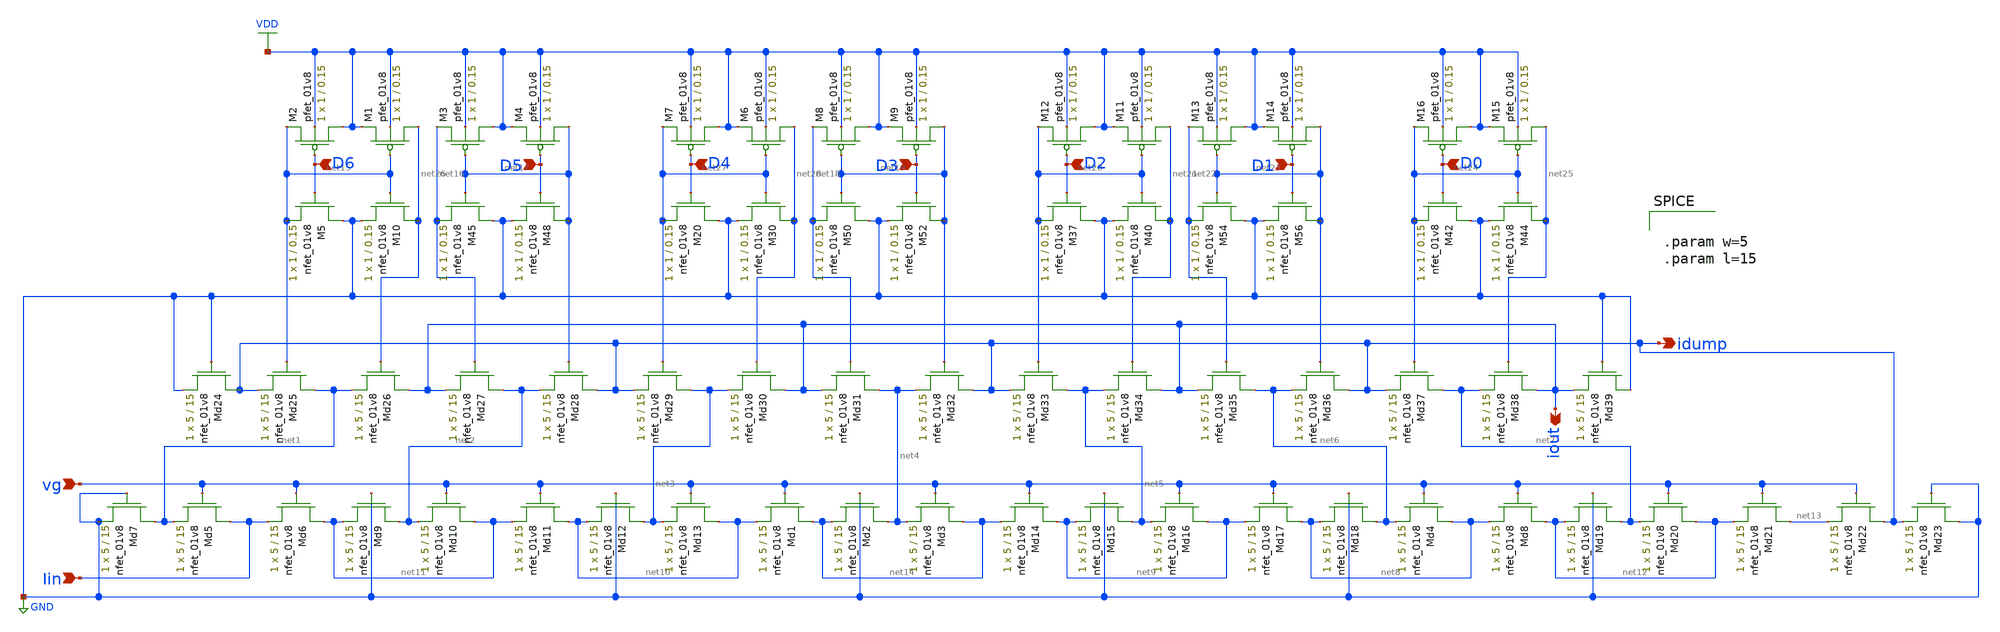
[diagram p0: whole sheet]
** sch_path: schematic/ladder_buffer_LDS4.sch
**.subckt ladder_buffer_LDS4 iout idump vg D0 D1 D3 D5 D6 Iin D4 D2
*.opin iout
*.opin idump
*.ipin vg
*.ipin D0
*.ipin D1
*.ipin D3
*.ipin D5
*.ipin D6
*.ipin Iin
*.ipin D4
*.ipin D2
XMd7 net1 GND GND GND sky130_fd_pr__nfet_01v8 L=15 W=5 nf=1 ad='int((nf+1)/2) * W/nf * 0.29' as='int((nf+2)/2) * W/nf * 0.29'
+ pd='2*int((nf+1)/2) * (W/nf + 0.29)' ps='2*int((nf+2)/2) * (W/nf + 0.29)' nrd='0.29 / W' nrs='0.29 / W'
+ sa=0 sb=0 sd=0 mult=1 m=1
XM5 GND D6 net15 GND sky130_fd_pr__nfet_01v8 L=0.15 W=1 nf=1 ad='int((nf+1)/2) * W/nf * 0.29' as='int((nf+2)/2) * W/nf * 0.29'
+ pd='2*int((nf+1)/2) * (W/nf + 0.29)' ps='2*int((nf+2)/2) * (W/nf + 0.29)' nrd='0.29 / W' nrs='0.29 / W'
+ sa=0 sb=0 sd=0 mult=1 m=1
XM10 net26 net15 GND GND sky130_fd_pr__nfet_01v8 L=0.15 W=1 nf=1 ad='int((nf+1)/2) * W/nf * 0.29' as='int((nf+2)/2) * W/nf * 0.29'
+ pd='2*int((nf+1)/2) * (W/nf + 0.29)' ps='2*int((nf+2)/2) * (W/nf + 0.29)' nrd='0.29 / W' nrs='0.29 / W'
+ sa=0 sb=0 sd=0 mult=1 m=1
XM20 GND D4 net27 GND sky130_fd_pr__nfet_01v8 L=0.15 W=1 nf=1 ad='int((nf+1)/2) * W/nf * 0.29' as='int((nf+2)/2) * W/nf * 0.29'
+ pd='2*int((nf+1)/2) * (W/nf + 0.29)' ps='2*int((nf+2)/2) * (W/nf + 0.29)' nrd='0.29 / W' nrs='0.29 / W'
+ sa=0 sb=0 sd=0 mult=1 m=1
XM30 net28 net27 GND GND sky130_fd_pr__nfet_01v8 L=0.15 W=1 nf=1 ad='int((nf+1)/2) * W/nf * 0.29' as='int((nf+2)/2) * W/nf * 0.29'
+ pd='2*int((nf+1)/2) * (W/nf + 0.29)' ps='2*int((nf+2)/2) * (W/nf + 0.29)' nrd='0.29 / W' nrs='0.29 / W'
+ sa=0 sb=0 sd=0 mult=1 m=1
XM37 GND D2 net20 GND sky130_fd_pr__nfet_01v8 L=0.15 W=1 nf=1 ad='int((nf+1)/2) * W/nf * 0.29' as='int((nf+2)/2) * W/nf * 0.29'
+ pd='2*int((nf+1)/2) * (W/nf + 0.29)' ps='2*int((nf+2)/2) * (W/nf + 0.29)' nrd='0.29 / W' nrs='0.29 / W'
+ sa=0 sb=0 sd=0 mult=1 m=1
XM40 net21 net20 GND GND sky130_fd_pr__nfet_01v8 L=0.15 W=1 nf=1 ad='int((nf+1)/2) * W/nf * 0.29' as='int((nf+2)/2) * W/nf * 0.29'
+ pd='2*int((nf+1)/2) * (W/nf + 0.29)' ps='2*int((nf+2)/2) * (W/nf + 0.29)' nrd='0.29 / W' nrs='0.29 / W'
+ sa=0 sb=0 sd=0 mult=1 m=1
XM42 GND D0 net24 GND sky130_fd_pr__nfet_01v8 L=0.15 W=1 nf=1 ad='int((nf+1)/2) * W/nf * 0.29' as='int((nf+2)/2) * W/nf * 0.29'
+ pd='2*int((nf+1)/2) * (W/nf + 0.29)' ps='2*int((nf+2)/2) * (W/nf + 0.29)' nrd='0.29 / W' nrs='0.29 / W'
+ sa=0 sb=0 sd=0 mult=1 m=1
XM44 net25 net24 GND GND sky130_fd_pr__nfet_01v8 L=0.15 W=1 nf=1 ad='int((nf+1)/2) * W/nf * 0.29' as='int((nf+2)/2) * W/nf * 0.29'
+ pd='2*int((nf+1)/2) * (W/nf + 0.29)' ps='2*int((nf+2)/2) * (W/nf + 0.29)' nrd='0.29 / W' nrs='0.29 / W'
+ sa=0 sb=0 sd=0 mult=1 m=1
XM45 GND net17 net16 GND sky130_fd_pr__nfet_01v8 L=0.15 W=1 nf=1 ad='int((nf+1)/2) * W/nf * 0.29' as='int((nf+2)/2) * W/nf * 0.29'
+ pd='2*int((nf+1)/2) * (W/nf + 0.29)' ps='2*int((nf+2)/2) * (W/nf + 0.29)' nrd='0.29 / W' nrs='0.29 / W'
+ sa=0 sb=0 sd=0 mult=1 m=1
XM48 net17 D5 GND GND sky130_fd_pr__nfet_01v8 L=0.15 W=1 nf=1 ad='int((nf+1)/2) * W/nf * 0.29' as='int((nf+2)/2) * W/nf * 0.29'
+ pd='2*int((nf+1)/2) * (W/nf + 0.29)' ps='2*int((nf+2)/2) * (W/nf + 0.29)' nrd='0.29 / W' nrs='0.29 / W'
+ sa=0 sb=0 sd=0 mult=1 m=1
XM50 GND net19 net18 GND sky130_fd_pr__nfet_01v8 L=0.15 W=1 nf=1 ad='int((nf+1)/2) * W/nf * 0.29' as='int((nf+2)/2) * W/nf * 0.29'
+ pd='2*int((nf+1)/2) * (W/nf + 0.29)' ps='2*int((nf+2)/2) * (W/nf + 0.29)' nrd='0.29 / W' nrs='0.29 / W'
+ sa=0 sb=0 sd=0 mult=1 m=1
XM52 net19 D3 GND GND sky130_fd_pr__nfet_01v8 L=0.15 W=1 nf=1 ad='int((nf+1)/2) * W/nf * 0.29' as='int((nf+2)/2) * W/nf * 0.29'
+ pd='2*int((nf+1)/2) * (W/nf + 0.29)' ps='2*int((nf+2)/2) * (W/nf + 0.29)' nrd='0.29 / W' nrs='0.29 / W'
+ sa=0 sb=0 sd=0 mult=1 m=1
XM54 GND net23 net22 GND sky130_fd_pr__nfet_01v8 L=0.15 W=1 nf=1 ad='int((nf+1)/2) * W/nf * 0.29' as='int((nf+2)/2) * W/nf * 0.29'
+ pd='2*int((nf+1)/2) * (W/nf + 0.29)' ps='2*int((nf+2)/2) * (W/nf + 0.29)' nrd='0.29 / W' nrs='0.29 / W'
+ sa=0 sb=0 sd=0 mult=1 m=1
XM56 net23 D1 GND GND sky130_fd_pr__nfet_01v8 L=0.15 W=1 nf=1 ad='int((nf+1)/2) * W/nf * 0.29' as='int((nf+2)/2) * W/nf * 0.29'
+ pd='2*int((nf+1)/2) * (W/nf + 0.29)' ps='2*int((nf+2)/2) * (W/nf + 0.29)' nrd='0.29 / W' nrs='0.29 / W'
+ sa=0 sb=0 sd=0 mult=1 m=1
XMd5 Iin vg net1 GND sky130_fd_pr__nfet_01v8 L=15 W=5 nf=1 ad='int((nf+1)/2) * W/nf * 0.29' as='int((nf+2)/2) * W/nf * 0.29'
+ pd='2*int((nf+1)/2) * (W/nf + 0.29)' ps='2*int((nf+2)/2) * (W/nf + 0.29)' nrd='0.29 / W' nrs='0.29 / W'
+ sa=0 sb=0 sd=0 mult=1 m=1
XMd6 net11 vg Iin GND sky130_fd_pr__nfet_01v8 L=15 W=5 nf=1 ad='int((nf+1)/2) * W/nf * 0.29' as='int((nf+2)/2) * W/nf * 0.29'
+ pd='2*int((nf+1)/2) * (W/nf + 0.29)' ps='2*int((nf+2)/2) * (W/nf + 0.29)' nrd='0.29 / W' nrs='0.29 / W'
+ sa=0 sb=0 sd=0 mult=1 m=1
XMd9 net2 GND net11 GND sky130_fd_pr__nfet_01v8 L=15 W=5 nf=1 ad='int((nf+1)/2) * W/nf * 0.29' as='int((nf+2)/2) * W/nf * 0.29'
+ pd='2*int((nf+1)/2) * (W/nf + 0.29)' ps='2*int((nf+2)/2) * (W/nf + 0.29)' nrd='0.29 / W' nrs='0.29 / W'
+ sa=0 sb=0 sd=0 mult=1 m=1
XMd10 net11 vg net2 GND sky130_fd_pr__nfet_01v8 L=15 W=5 nf=1 ad='int((nf+1)/2) * W/nf * 0.29' as='int((nf+2)/2) * W/nf * 0.29'
+ pd='2*int((nf+1)/2) * (W/nf + 0.29)' ps='2*int((nf+2)/2) * (W/nf + 0.29)' nrd='0.29 / W' nrs='0.29 / W'
+ sa=0 sb=0 sd=0 mult=1 m=1
XMd11 net10 vg net11 GND sky130_fd_pr__nfet_01v8 L=15 W=5 nf=1 ad='int((nf+1)/2) * W/nf * 0.29' as='int((nf+2)/2) * W/nf * 0.29'
+ pd='2*int((nf+1)/2) * (W/nf + 0.29)' ps='2*int((nf+2)/2) * (W/nf + 0.29)' nrd='0.29 / W' nrs='0.29 / W'
+ sa=0 sb=0 sd=0 mult=1 m=1
XMd12 net3 GND net10 GND sky130_fd_pr__nfet_01v8 L=15 W=5 nf=1 ad='int((nf+1)/2) * W/nf * 0.29' as='int((nf+2)/2) * W/nf * 0.29'
+ pd='2*int((nf+1)/2) * (W/nf + 0.29)' ps='2*int((nf+2)/2) * (W/nf + 0.29)' nrd='0.29 / W' nrs='0.29 / W'
+ sa=0 sb=0 sd=0 mult=1 m=1
XMd13 net10 vg net3 GND sky130_fd_pr__nfet_01v8 L=15 W=5 nf=1 ad='int((nf+1)/2) * W/nf * 0.29' as='int((nf+2)/2) * W/nf * 0.29'
+ pd='2*int((nf+1)/2) * (W/nf + 0.29)' ps='2*int((nf+2)/2) * (W/nf + 0.29)' nrd='0.29 / W' nrs='0.29 / W'
+ sa=0 sb=0 sd=0 mult=1 m=1
XMd1 net14 vg net10 GND sky130_fd_pr__nfet_01v8 L=15 W=5 nf=1 ad='int((nf+1)/2) * W/nf * 0.29' as='int((nf+2)/2) * W/nf * 0.29'
+ pd='2*int((nf+1)/2) * (W/nf + 0.29)' ps='2*int((nf+2)/2) * (W/nf + 0.29)' nrd='0.29 / W' nrs='0.29 / W'
+ sa=0 sb=0 sd=0 mult=1 m=1
XMd2 net4 GND net14 GND sky130_fd_pr__nfet_01v8 L=15 W=5 nf=1 ad='int((nf+1)/2) * W/nf * 0.29' as='int((nf+2)/2) * W/nf * 0.29'
+ pd='2*int((nf+1)/2) * (W/nf + 0.29)' ps='2*int((nf+2)/2) * (W/nf + 0.29)' nrd='0.29 / W' nrs='0.29 / W'
+ sa=0 sb=0 sd=0 mult=1 m=1
XMd3 net14 vg net4 GND sky130_fd_pr__nfet_01v8 L=15 W=5 nf=1 ad='int((nf+1)/2) * W/nf * 0.29' as='int((nf+2)/2) * W/nf * 0.29'
+ pd='2*int((nf+1)/2) * (W/nf + 0.29)' ps='2*int((nf+2)/2) * (W/nf + 0.29)' nrd='0.29 / W' nrs='0.29 / W'
+ sa=0 sb=0 sd=0 mult=1 m=1
XMd14 net9 vg net14 GND sky130_fd_pr__nfet_01v8 L=15 W=5 nf=1 ad='int((nf+1)/2) * W/nf * 0.29' as='int((nf+2)/2) * W/nf * 0.29'
+ pd='2*int((nf+1)/2) * (W/nf + 0.29)' ps='2*int((nf+2)/2) * (W/nf + 0.29)' nrd='0.29 / W' nrs='0.29 / W'
+ sa=0 sb=0 sd=0 mult=1 m=1
XMd15 net5 GND net9 GND sky130_fd_pr__nfet_01v8 L=15 W=5 nf=1 ad='int((nf+1)/2) * W/nf * 0.29' as='int((nf+2)/2) * W/nf * 0.29'
+ pd='2*int((nf+1)/2) * (W/nf + 0.29)' ps='2*int((nf+2)/2) * (W/nf + 0.29)' nrd='0.29 / W' nrs='0.29 / W'
+ sa=0 sb=0 sd=0 mult=1 m=1
XMd16 net9 vg net5 GND sky130_fd_pr__nfet_01v8 L=15 W=5 nf=1 ad='int((nf+1)/2) * W/nf * 0.29' as='int((nf+2)/2) * W/nf * 0.29'
+ pd='2*int((nf+1)/2) * (W/nf + 0.29)' ps='2*int((nf+2)/2) * (W/nf + 0.29)' nrd='0.29 / W' nrs='0.29 / W'
+ sa=0 sb=0 sd=0 mult=1 m=1
XMd17 net8 vg net9 GND sky130_fd_pr__nfet_01v8 L=15 W=5 nf=1 ad='int((nf+1)/2) * W/nf * 0.29' as='int((nf+2)/2) * W/nf * 0.29'
+ pd='2*int((nf+1)/2) * (W/nf + 0.29)' ps='2*int((nf+2)/2) * (W/nf + 0.29)' nrd='0.29 / W' nrs='0.29 / W'
+ sa=0 sb=0 sd=0 mult=1 m=1
XMd18 net6 GND net8 GND sky130_fd_pr__nfet_01v8 L=15 W=5 nf=1 ad='int((nf+1)/2) * W/nf * 0.29' as='int((nf+2)/2) * W/nf * 0.29'
+ pd='2*int((nf+1)/2) * (W/nf + 0.29)' ps='2*int((nf+2)/2) * (W/nf + 0.29)' nrd='0.29 / W' nrs='0.29 / W'
+ sa=0 sb=0 sd=0 mult=1 m=1
XMd4 net8 vg net6 GND sky130_fd_pr__nfet_01v8 L=15 W=5 nf=1 ad='int((nf+1)/2) * W/nf * 0.29' as='int((nf+2)/2) * W/nf * 0.29'
+ pd='2*int((nf+1)/2) * (W/nf + 0.29)' ps='2*int((nf+2)/2) * (W/nf + 0.29)' nrd='0.29 / W' nrs='0.29 / W'
+ sa=0 sb=0 sd=0 mult=1 m=1
XMd8 net12 vg net8 GND sky130_fd_pr__nfet_01v8 L=15 W=5 nf=1 ad='int((nf+1)/2) * W/nf * 0.29' as='int((nf+2)/2) * W/nf * 0.29'
+ pd='2*int((nf+1)/2) * (W/nf + 0.29)' ps='2*int((nf+2)/2) * (W/nf + 0.29)' nrd='0.29 / W' nrs='0.29 / W'
+ sa=0 sb=0 sd=0 mult=1 m=1
XMd19 net7 GND net12 GND sky130_fd_pr__nfet_01v8 L=15 W=5 nf=1 ad='int((nf+1)/2) * W/nf * 0.29' as='int((nf+2)/2) * W/nf * 0.29'
+ pd='2*int((nf+1)/2) * (W/nf + 0.29)' ps='2*int((nf+2)/2) * (W/nf + 0.29)' nrd='0.29 / W' nrs='0.29 / W'
+ sa=0 sb=0 sd=0 mult=1 m=1
XMd20 net12 vg net7 GND sky130_fd_pr__nfet_01v8 L=15 W=5 nf=1 ad='int((nf+1)/2) * W/nf * 0.29' as='int((nf+2)/2) * W/nf * 0.29'
+ pd='2*int((nf+1)/2) * (W/nf + 0.29)' ps='2*int((nf+2)/2) * (W/nf + 0.29)' nrd='0.29 / W' nrs='0.29 / W'
+ sa=0 sb=0 sd=0 mult=1 m=1
XMd21 net13 vg net12 GND sky130_fd_pr__nfet_01v8 L=15 W=5 nf=1 ad='int((nf+1)/2) * W/nf * 0.29' as='int((nf+2)/2) * W/nf * 0.29'
+ pd='2*int((nf+1)/2) * (W/nf + 0.29)' ps='2*int((nf+2)/2) * (W/nf + 0.29)' nrd='0.29 / W' nrs='0.29 / W'
+ sa=0 sb=0 sd=0 mult=1 m=1
XMd22 idump vg net13 GND sky130_fd_pr__nfet_01v8 L=15 W=5 nf=1 ad='int((nf+1)/2) * W/nf * 0.29' as='int((nf+2)/2) * W/nf * 0.29'
+ pd='2*int((nf+1)/2) * (W/nf + 0.29)' ps='2*int((nf+2)/2) * (W/nf + 0.29)' nrd='0.29 / W' nrs='0.29 / W'
+ sa=0 sb=0 sd=0 mult=1 m=1
XMd23 GND GND idump GND sky130_fd_pr__nfet_01v8 L=15 W=5 nf=1 ad='int((nf+1)/2) * W/nf * 0.29' as='int((nf+2)/2) * W/nf * 0.29'
+ pd='2*int((nf+1)/2) * (W/nf + 0.29)' ps='2*int((nf+2)/2) * (W/nf + 0.29)' nrd='0.29 / W' nrs='0.29 / W'
+ sa=0 sb=0 sd=0 mult=1 m=1
XMd24 idump GND GND GND sky130_fd_pr__nfet_01v8 L=15 W=5 nf=1 ad='int((nf+1)/2) * W/nf * 0.29' as='int((nf+2)/2) * W/nf * 0.29'
+ pd='2*int((nf+1)/2) * (W/nf + 0.29)' ps='2*int((nf+2)/2) * (W/nf + 0.29)' nrd='0.29 / W' nrs='0.29 / W'
+ sa=0 sb=0 sd=0 mult=1 m=1
XMd25 net1 net15 idump GND sky130_fd_pr__nfet_01v8 L=15 W=5 nf=1 ad='int((nf+1)/2) * W/nf * 0.29' as='int((nf+2)/2) * W/nf * 0.29'
+ pd='2*int((nf+1)/2) * (W/nf + 0.29)' ps='2*int((nf+2)/2) * (W/nf + 0.29)' nrd='0.29 / W' nrs='0.29 / W'
+ sa=0 sb=0 sd=0 mult=1 m=1
XMd26 iout net26 net1 GND sky130_fd_pr__nfet_01v8 L=15 W=5 nf=1 ad='int((nf+1)/2) * W/nf * 0.29' as='int((nf+2)/2) * W/nf * 0.29'
+ pd='2*int((nf+1)/2) * (W/nf + 0.29)' ps='2*int((nf+2)/2) * (W/nf + 0.29)' nrd='0.29 / W' nrs='0.29 / W'
+ sa=0 sb=0 sd=0 mult=1 m=1
XMd27 net2 net16 iout GND sky130_fd_pr__nfet_01v8 L=15 W=5 nf=1 ad='int((nf+1)/2) * W/nf * 0.29' as='int((nf+2)/2) * W/nf * 0.29'
+ pd='2*int((nf+1)/2) * (W/nf + 0.29)' ps='2*int((nf+2)/2) * (W/nf + 0.29)' nrd='0.29 / W' nrs='0.29 / W'
+ sa=0 sb=0 sd=0 mult=1 m=1
XMd28 idump net17 net2 GND sky130_fd_pr__nfet_01v8 L=15 W=5 nf=1 ad='int((nf+1)/2) * W/nf * 0.29' as='int((nf+2)/2) * W/nf * 0.29'
+ pd='2*int((nf+1)/2) * (W/nf + 0.29)' ps='2*int((nf+2)/2) * (W/nf + 0.29)' nrd='0.29 / W' nrs='0.29 / W'
+ sa=0 sb=0 sd=0 mult=1 m=1
XMd29 net3 net27 idump GND sky130_fd_pr__nfet_01v8 L=15 W=5 nf=1 ad='int((nf+1)/2) * W/nf * 0.29' as='int((nf+2)/2) * W/nf * 0.29'
+ pd='2*int((nf+1)/2) * (W/nf + 0.29)' ps='2*int((nf+2)/2) * (W/nf + 0.29)' nrd='0.29 / W' nrs='0.29 / W'
+ sa=0 sb=0 sd=0 mult=1 m=1
XMd30 iout net28 net3 GND sky130_fd_pr__nfet_01v8 L=15 W=5 nf=1 ad='int((nf+1)/2) * W/nf * 0.29' as='int((nf+2)/2) * W/nf * 0.29'
+ pd='2*int((nf+1)/2) * (W/nf + 0.29)' ps='2*int((nf+2)/2) * (W/nf + 0.29)' nrd='0.29 / W' nrs='0.29 / W'
+ sa=0 sb=0 sd=0 mult=1 m=1
XMd31 net4 net18 iout GND sky130_fd_pr__nfet_01v8 L=15 W=5 nf=1 ad='int((nf+1)/2) * W/nf * 0.29' as='int((nf+2)/2) * W/nf * 0.29'
+ pd='2*int((nf+1)/2) * (W/nf + 0.29)' ps='2*int((nf+2)/2) * (W/nf + 0.29)' nrd='0.29 / W' nrs='0.29 / W'
+ sa=0 sb=0 sd=0 mult=1 m=1
XMd32 idump net19 net4 GND sky130_fd_pr__nfet_01v8 L=15 W=5 nf=1 ad='int((nf+1)/2) * W/nf * 0.29' as='int((nf+2)/2) * W/nf * 0.29'
+ pd='2*int((nf+1)/2) * (W/nf + 0.29)' ps='2*int((nf+2)/2) * (W/nf + 0.29)' nrd='0.29 / W' nrs='0.29 / W'
+ sa=0 sb=0 sd=0 mult=1 m=1
XMd33 net5 net20 idump GND sky130_fd_pr__nfet_01v8 L=15 W=5 nf=1 ad='int((nf+1)/2) * W/nf * 0.29' as='int((nf+2)/2) * W/nf * 0.29'
+ pd='2*int((nf+1)/2) * (W/nf + 0.29)' ps='2*int((nf+2)/2) * (W/nf + 0.29)' nrd='0.29 / W' nrs='0.29 / W'
+ sa=0 sb=0 sd=0 mult=1 m=1
XMd34 iout net21 net5 GND sky130_fd_pr__nfet_01v8 L=15 W=5 nf=1 ad='int((nf+1)/2) * W/nf * 0.29' as='int((nf+2)/2) * W/nf * 0.29'
+ pd='2*int((nf+1)/2) * (W/nf + 0.29)' ps='2*int((nf+2)/2) * (W/nf + 0.29)' nrd='0.29 / W' nrs='0.29 / W'
+ sa=0 sb=0 sd=0 mult=1 m=1
XMd35 net6 net22 iout GND sky130_fd_pr__nfet_01v8 L=15 W=5 nf=1 ad='int((nf+1)/2) * W/nf * 0.29' as='int((nf+2)/2) * W/nf * 0.29'
+ pd='2*int((nf+1)/2) * (W/nf + 0.29)' ps='2*int((nf+2)/2) * (W/nf + 0.29)' nrd='0.29 / W' nrs='0.29 / W'
+ sa=0 sb=0 sd=0 mult=1 m=1
XMd36 idump net23 net6 GND sky130_fd_pr__nfet_01v8 L=15 W=5 nf=1 ad='int((nf+1)/2) * W/nf * 0.29' as='int((nf+2)/2) * W/nf * 0.29'
+ pd='2*int((nf+1)/2) * (W/nf + 0.29)' ps='2*int((nf+2)/2) * (W/nf + 0.29)' nrd='0.29 / W' nrs='0.29 / W'
+ sa=0 sb=0 sd=0 mult=1 m=1
XMd37 net7 net24 idump GND sky130_fd_pr__nfet_01v8 L=15 W=5 nf=1 ad='int((nf+1)/2) * W/nf * 0.29' as='int((nf+2)/2) * W/nf * 0.29'
+ pd='2*int((nf+1)/2) * (W/nf + 0.29)' ps='2*int((nf+2)/2) * (W/nf + 0.29)' nrd='0.29 / W' nrs='0.29 / W'
+ sa=0 sb=0 sd=0 mult=1 m=1
XMd38 iout net25 net7 GND sky130_fd_pr__nfet_01v8 L=15 W=5 nf=1 ad='int((nf+1)/2) * W/nf * 0.29' as='int((nf+2)/2) * W/nf * 0.29'
+ pd='2*int((nf+1)/2) * (W/nf + 0.29)' ps='2*int((nf+2)/2) * (W/nf + 0.29)' nrd='0.29 / W' nrs='0.29 / W'
+ sa=0 sb=0 sd=0 mult=1 m=1
XMd39 GND GND iout GND sky130_fd_pr__nfet_01v8 L=15 W=5 nf=1 ad='int((nf+1)/2) * W/nf * 0.29' as='int((nf+2)/2) * W/nf * 0.29'
+ pd='2*int((nf+1)/2) * (W/nf + 0.29)' ps='2*int((nf+2)/2) * (W/nf + 0.29)' nrd='0.29 / W' nrs='0.29 / W'
+ sa=0 sb=0 sd=0 mult=1 m=1
XM1 net26 net15 VDD VDD sky130_fd_pr__pfet_01v8 L=0.15 W=1 nf=1 ad='int((nf+1)/2) * W/nf * 0.29' as='int((nf+2)/2) * W/nf * 0.29'
+ pd='2*int((nf+1)/2) * (W/nf + 0.29)' ps='2*int((nf+2)/2) * (W/nf + 0.29)' nrd='0.29 / W' nrs='0.29 / W'
+ sa=0 sb=0 sd=0 mult=1 m=1
XM2 VDD D6 net15 VDD sky130_fd_pr__pfet_01v8 L=0.15 W=1 nf=1 ad='int((nf+1)/2) * W/nf * 0.29' as='int((nf+2)/2) * W/nf * 0.29'
+ pd='2*int((nf+1)/2) * (W/nf + 0.29)' ps='2*int((nf+2)/2) * (W/nf + 0.29)' nrd='0.29 / W' nrs='0.29 / W'
+ sa=0 sb=0 sd=0 mult=1 m=1
XM3 VDD net17 net16 VDD sky130_fd_pr__pfet_01v8 L=0.15 W=1 nf=1 ad='int((nf+1)/2) * W/nf * 0.29' as='int((nf+2)/2) * W/nf * 0.29'
+ pd='2*int((nf+1)/2) * (W/nf + 0.29)' ps='2*int((nf+2)/2) * (W/nf + 0.29)' nrd='0.29 / W' nrs='0.29 / W'
+ sa=0 sb=0 sd=0 mult=1 m=1
XM4 net17 D5 VDD VDD sky130_fd_pr__pfet_01v8 L=0.15 W=1 nf=1 ad='int((nf+1)/2) * W/nf * 0.29' as='int((nf+2)/2) * W/nf * 0.29'
+ pd='2*int((nf+1)/2) * (W/nf + 0.29)' ps='2*int((nf+2)/2) * (W/nf + 0.29)' nrd='0.29 / W' nrs='0.29 / W'
+ sa=0 sb=0 sd=0 mult=1 m=1
XM6 net28 net27 VDD VDD sky130_fd_pr__pfet_01v8 L=0.15 W=1 nf=1 ad='int((nf+1)/2) * W/nf * 0.29' as='int((nf+2)/2) * W/nf * 0.29'
+ pd='2*int((nf+1)/2) * (W/nf + 0.29)' ps='2*int((nf+2)/2) * (W/nf + 0.29)' nrd='0.29 / W' nrs='0.29 / W'
+ sa=0 sb=0 sd=0 mult=1 m=1
XM7 VDD D4 net27 VDD sky130_fd_pr__pfet_01v8 L=0.15 W=1 nf=1 ad='int((nf+1)/2) * W/nf * 0.29' as='int((nf+2)/2) * W/nf * 0.29'
+ pd='2*int((nf+1)/2) * (W/nf + 0.29)' ps='2*int((nf+2)/2) * (W/nf + 0.29)' nrd='0.29 / W' nrs='0.29 / W'
+ sa=0 sb=0 sd=0 mult=1 m=1
XM8 VDD net19 net18 VDD sky130_fd_pr__pfet_01v8 L=0.15 W=1 nf=1 ad='int((nf+1)/2) * W/nf * 0.29' as='int((nf+2)/2) * W/nf * 0.29'
+ pd='2*int((nf+1)/2) * (W/nf + 0.29)' ps='2*int((nf+2)/2) * (W/nf + 0.29)' nrd='0.29 / W' nrs='0.29 / W'
+ sa=0 sb=0 sd=0 mult=1 m=1
XM9 net19 D3 VDD VDD sky130_fd_pr__pfet_01v8 L=0.15 W=1 nf=1 ad='int((nf+1)/2) * W/nf * 0.29' as='int((nf+2)/2) * W/nf * 0.29'
+ pd='2*int((nf+1)/2) * (W/nf + 0.29)' ps='2*int((nf+2)/2) * (W/nf + 0.29)' nrd='0.29 / W' nrs='0.29 / W'
+ sa=0 sb=0 sd=0 mult=1 m=1
XM11 net21 net20 VDD VDD sky130_fd_pr__pfet_01v8 L=0.15 W=1 nf=1 ad='int((nf+1)/2) * W/nf * 0.29' as='int((nf+2)/2) * W/nf * 0.29'
+ pd='2*int((nf+1)/2) * (W/nf + 0.29)' ps='2*int((nf+2)/2) * (W/nf + 0.29)' nrd='0.29 / W' nrs='0.29 / W'
+ sa=0 sb=0 sd=0 mult=1 m=1
XM12 VDD D2 net20 VDD sky130_fd_pr__pfet_01v8 L=0.15 W=1 nf=1 ad='int((nf+1)/2) * W/nf * 0.29' as='int((nf+2)/2) * W/nf * 0.29'
+ pd='2*int((nf+1)/2) * (W/nf + 0.29)' ps='2*int((nf+2)/2) * (W/nf + 0.29)' nrd='0.29 / W' nrs='0.29 / W'
+ sa=0 sb=0 sd=0 mult=1 m=1
XM13 VDD net23 net22 VDD sky130_fd_pr__pfet_01v8 L=0.15 W=1 nf=1 ad='int((nf+1)/2) * W/nf * 0.29' as='int((nf+2)/2) * W/nf * 0.29'
+ pd='2*int((nf+1)/2) * (W/nf + 0.29)' ps='2*int((nf+2)/2) * (W/nf + 0.29)' nrd='0.29 / W' nrs='0.29 / W'
+ sa=0 sb=0 sd=0 mult=1 m=1
XM14 net23 D1 VDD VDD sky130_fd_pr__pfet_01v8 L=0.15 W=1 nf=1 ad='int((nf+1)/2) * W/nf * 0.29' as='int((nf+2)/2) * W/nf * 0.29'
+ pd='2*int((nf+1)/2) * (W/nf + 0.29)' ps='2*int((nf+2)/2) * (W/nf + 0.29)' nrd='0.29 / W' nrs='0.29 / W'
+ sa=0 sb=0 sd=0 mult=1 m=1
XM15 net25 net24 VDD VDD sky130_fd_pr__pfet_01v8 L=0.15 W=1 nf=1 ad='int((nf+1)/2) * W/nf * 0.29' as='int((nf+2)/2) * W/nf * 0.29'
+ pd='2*int((nf+1)/2) * (W/nf + 0.29)' ps='2*int((nf+2)/2) * (W/nf + 0.29)' nrd='0.29 / W' nrs='0.29 / W'
+ sa=0 sb=0 sd=0 mult=1 m=1
XM16 VDD D0 net24 VDD sky130_fd_pr__pfet_01v8 L=0.15 W=1 nf=1 ad='int((nf+1)/2) * W/nf * 0.29' as='int((nf+2)/2) * W/nf * 0.29'
+ pd='2*int((nf+1)/2) * (W/nf + 0.29)' ps='2*int((nf+2)/2) * (W/nf + 0.29)' nrd='0.29 / W' nrs='0.29 / W'
+ sa=0 sb=0 sd=0 mult=1 m=1
**** begin user architecture code


.param w=5
.param l=15


**** end user architecture code
**.ends
.GLOBAL GND
.GLOBAL VDD
.end
